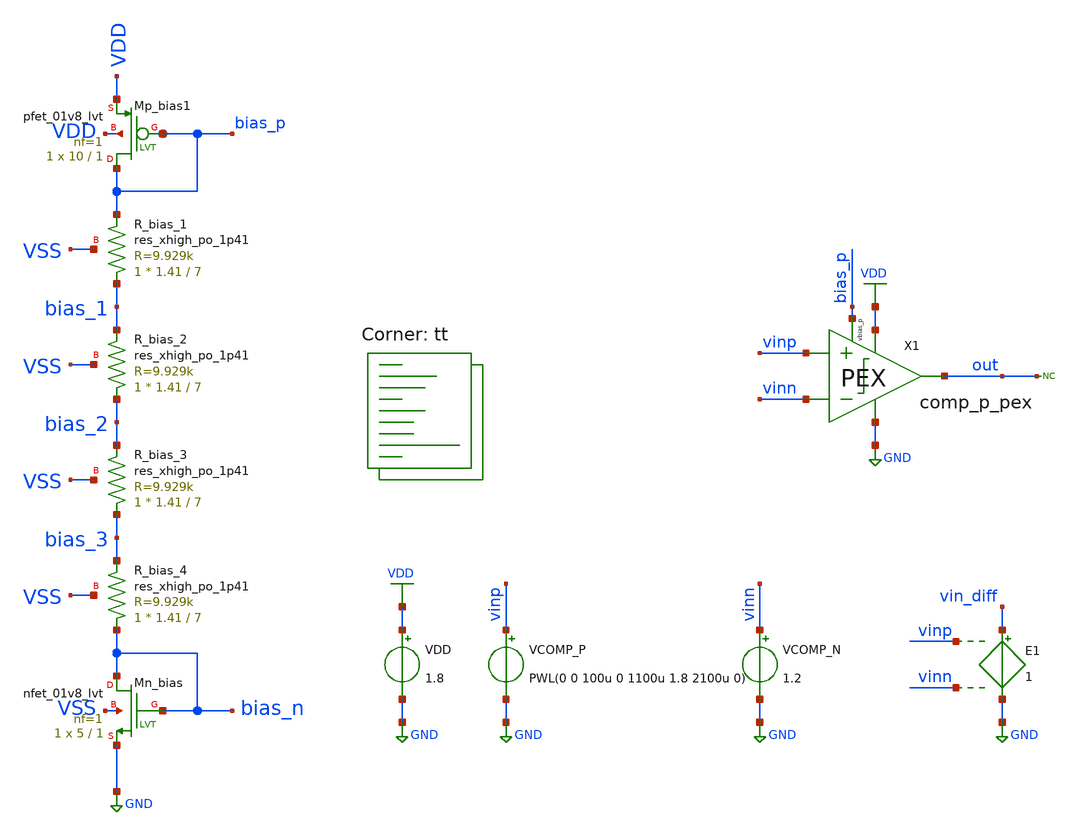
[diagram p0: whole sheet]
** sch_path: xsch/tb/comp_p/tb_comp_p_tran_sweep_pex.sch
**.subckt tb_comp_p_tran_sweep_pex
VDD VDD GND 1.8
* noconn out
VCOMP_N vinn GND 1.2
VCOMP_P vinp GND PWL(0 0 100u 0 1100u 1.8 2100u 0)
E1 vin_diff GND vinp vinn 1
XR_bias_1 bias_1 bias_p VSS sky130_fd_pr__res_xhigh_po_1p41 L=7 mult=1 m=1
XMn_bias bias_n bias_n GND VSS sky130_fd_pr__nfet_01v8_lvt L=1 W=5 nf=1 ad='int((nf+1)/2) * W/nf * 0.29'
+ as='int((nf+2)/2) * W/nf * 0.29' pd='2*int((nf+1)/2) * (W/nf + 0.29)' ps='2*int((nf+2)/2) * (W/nf + 0.29)'
+ nrd='0.29 / W' nrs='0.29 / W' sa=0 sb=0 sd=0 mult=1 m=1
XMp_bias1 bias_p bias_p VDD VDD sky130_fd_pr__pfet_01v8_lvt L=1 W=10 nf=1 ad='int((nf+1)/2) * W/nf * 0.29'
+ as='int((nf+2)/2) * W/nf * 0.29' pd='2*int((nf+1)/2) * (W/nf + 0.29)' ps='2*int((nf+2)/2) * (W/nf + 0.29)'
+ nrd='0.29 / W' nrs='0.29 / W' sa=0 sb=0 sd=0 mult=1 m=1
XR_bias_2 bias_2 bias_1 VSS sky130_fd_pr__res_xhigh_po_1p41 L=7 mult=1 m=1
XR_bias_3 bias_3 bias_2 VSS sky130_fd_pr__res_xhigh_po_1p41 L=7 mult=1 m=1
XR_bias_4 bias_n bias_3 VSS sky130_fd_pr__res_xhigh_po_1p41 L=7 mult=1 m=1
X1 vinp out VDD GND vinn bias_p comp_p_pex
**** begin user architecture code



* control language script
.save X_COMP_P.latch_right
.save X_COMP_P.latch_left
.save vinp vinn out vdd
.save X_COMP_P.tail

.control
tran 0.1u 2100u

meas tran v_cross_lh FIND v(vinp) when v(out)=0.9 RISE=1
meas tran v_cross_hl FIND v(vinp) when v(out)=0.9 FALL=1

let v_th = v_cross_lh-0.6
let v_tl = v_cross_hl-0.6
let v_hyst = $&v_th - $&v_tl
let v_offset = $&v_th + $&v_tl

set xbrushwidth=2
plot v(out) v(vinp) v(vinn)
plot v(x_comp_p.latch_right) v(x_comp_p.latch_left)
plot v(X_COMP_P.tail)

echo V_th: $&v_th
echo V_tl: $&v_tl
echo V_hyst: $&v_hyst
echo V_offset: $&v_offset

rusage

.endc
.end



.lib $::SKYWATER_MODELS/sky130.lib.spice tt


.include ~/projects/tt06_555/xsch/ip/comparators/comp_p/comp_p_pex.spice


**** end user architecture code
**.ends
.GLOBAL VDD
.GLOBAL GND
.end
